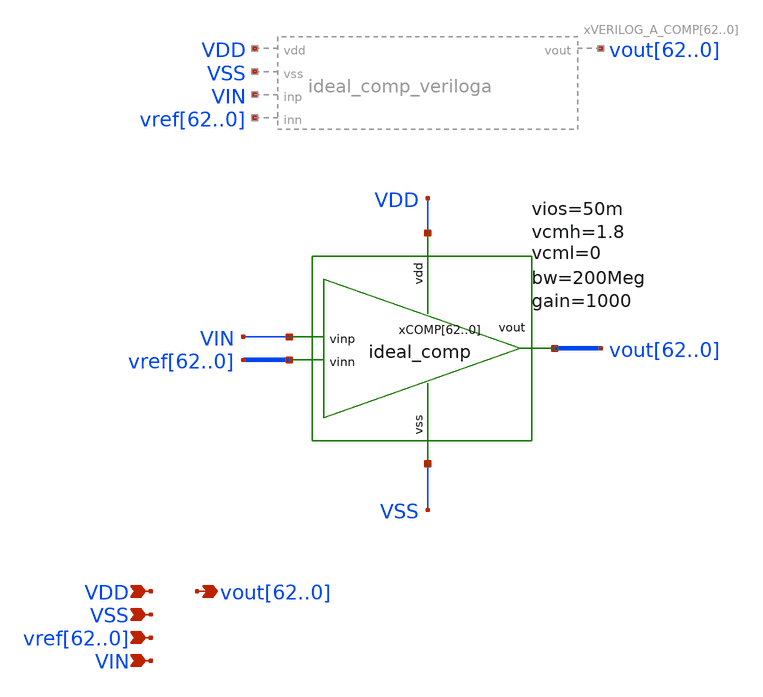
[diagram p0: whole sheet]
** sch_path: schematics/comp_top_ideal.sch
**.subckt comp_top_ideal
*+ vout62,vout61,vout60,vout59,vout58,vout57,vout56,vout55,vout54,vout53,vout52,vout51,vout50,vout49,vout48,vout47,vout46,vout45,vout44,vout43,vout42,vout41,vout40,vout39,vout38,vout37,vout36,vout35,vout34,vout33,vout32,vout31,vout30,vout29,vout28,vout27,vout26,vout25,vout24,vout23,vout22,vout21,vout20,vout19,vout18,vout17,vout16,vout15,vout14,vout13,vout12,vout11,vout10,vout9,vout8,vout7,vout6,vout5,vout4,vout3,vout2,vout1,vout0 VDD VSS
*+ vref62,vref61,vref60,vref59,vref58,vref57,vref56,vref55,vref54,vref53,vref52,vref51,vref50,vref49,vref48,vref47,vref46,vref45,vref44,vref43,vref42,vref41,vref40,vref39,vref38,vref37,vref36,vref35,vref34,vref33,vref32,vref31,vref30,vref29,vref28,vref27,vref26,vref25,vref24,vref23,vref22,vref21,vref20,vref19,vref18,vref17,vref16,vref15,vref14,vref13,vref12,vref11,vref10,vref9,vref8,vref7,vref6,vref5,vref4,vref3,vref2,vref1,vref0 VIN
*.opin
*+ vout62,vout61,vout60,vout59,vout58,vout57,vout56,vout55,vout54,vout53,vout52,vout51,vout50,vout49,vout48,vout47,vout46,vout45,vout44,vout43,vout42,vout41,vout40,vout39,vout38,vout37,vout36,vout35,vout34,vout33,vout32,vout31,vout30,vout29,vout28,vout27,vout26,vout25,vout24,vout23,vout22,vout21,vout20,vout19,vout18,vout17,vout16,vout15,vout14,vout13,vout12,vout11,vout10,vout9,vout8,vout7,vout6,vout5,vout4,vout3,vout2,vout1,vout0
*.ipin VDD
*.ipin VSS
*.ipin
*+ vref62,vref61,vref60,vref59,vref58,vref57,vref56,vref55,vref54,vref53,vref52,vref51,vref50,vref49,vref48,vref47,vref46,vref45,vref44,vref43,vref42,vref41,vref40,vref39,vref38,vref37,vref36,vref35,vref34,vref33,vref32,vref31,vref30,vref29,vref28,vref27,vref26,vref25,vref24,vref23,vref22,vref21,vref20,vref19,vref18,vref17,vref16,vref15,vref14,vref13,vref12,vref11,vref10,vref9,vref8,vref7,vref6,vref5,vref4,vref3,vref2,vref1,vref0
*.ipin VIN
xCOMP62 VDD VSS VIN vout62 vref62 ideal_comp bw=200Meg gain=1000 vdd= vss= vcmh=1.8 vcml=0 vios=50m
xCOMP61 VDD VSS VIN vout61 vref61 ideal_comp bw=200Meg gain=1000 vdd= vss= vcmh=1.8 vcml=0 vios=50m
xCOMP60 VDD VSS VIN vout60 vref60 ideal_comp bw=200Meg gain=1000 vdd= vss= vcmh=1.8 vcml=0 vios=50m
xCOMP59 VDD VSS VIN vout59 vref59 ideal_comp bw=200Meg gain=1000 vdd= vss= vcmh=1.8 vcml=0 vios=50m
xCOMP58 VDD VSS VIN vout58 vref58 ideal_comp bw=200Meg gain=1000 vdd= vss= vcmh=1.8 vcml=0 vios=50m
xCOMP57 VDD VSS VIN vout57 vref57 ideal_comp bw=200Meg gain=1000 vdd= vss= vcmh=1.8 vcml=0 vios=50m
xCOMP56 VDD VSS VIN vout56 vref56 ideal_comp bw=200Meg gain=1000 vdd= vss= vcmh=1.8 vcml=0 vios=50m
xCOMP55 VDD VSS VIN vout55 vref55 ideal_comp bw=200Meg gain=1000 vdd= vss= vcmh=1.8 vcml=0 vios=50m
xCOMP54 VDD VSS VIN vout54 vref54 ideal_comp bw=200Meg gain=1000 vdd= vss= vcmh=1.8 vcml=0 vios=50m
xCOMP53 VDD VSS VIN vout53 vref53 ideal_comp bw=200Meg gain=1000 vdd= vss= vcmh=1.8 vcml=0 vios=50m
xCOMP52 VDD VSS VIN vout52 vref52 ideal_comp bw=200Meg gain=1000 vdd= vss= vcmh=1.8 vcml=0 vios=50m
xCOMP51 VDD VSS VIN vout51 vref51 ideal_comp bw=200Meg gain=1000 vdd= vss= vcmh=1.8 vcml=0 vios=50m
xCOMP50 VDD VSS VIN vout50 vref50 ideal_comp bw=200Meg gain=1000 vdd= vss= vcmh=1.8 vcml=0 vios=50m
xCOMP49 VDD VSS VIN vout49 vref49 ideal_comp bw=200Meg gain=1000 vdd= vss= vcmh=1.8 vcml=0 vios=50m
xCOMP48 VDD VSS VIN vout48 vref48 ideal_comp bw=200Meg gain=1000 vdd= vss= vcmh=1.8 vcml=0 vios=50m
xCOMP47 VDD VSS VIN vout47 vref47 ideal_comp bw=200Meg gain=1000 vdd= vss= vcmh=1.8 vcml=0 vios=50m
xCOMP46 VDD VSS VIN vout46 vref46 ideal_comp bw=200Meg gain=1000 vdd= vss= vcmh=1.8 vcml=0 vios=50m
xCOMP45 VDD VSS VIN vout45 vref45 ideal_comp bw=200Meg gain=1000 vdd= vss= vcmh=1.8 vcml=0 vios=50m
xCOMP44 VDD VSS VIN vout44 vref44 ideal_comp bw=200Meg gain=1000 vdd= vss= vcmh=1.8 vcml=0 vios=50m
xCOMP43 VDD VSS VIN vout43 vref43 ideal_comp bw=200Meg gain=1000 vdd= vss= vcmh=1.8 vcml=0 vios=50m
xCOMP42 VDD VSS VIN vout42 vref42 ideal_comp bw=200Meg gain=1000 vdd= vss= vcmh=1.8 vcml=0 vios=50m
xCOMP41 VDD VSS VIN vout41 vref41 ideal_comp bw=200Meg gain=1000 vdd= vss= vcmh=1.8 vcml=0 vios=50m
xCOMP40 VDD VSS VIN vout40 vref40 ideal_comp bw=200Meg gain=1000 vdd= vss= vcmh=1.8 vcml=0 vios=50m
xCOMP39 VDD VSS VIN vout39 vref39 ideal_comp bw=200Meg gain=1000 vdd= vss= vcmh=1.8 vcml=0 vios=50m
xCOMP38 VDD VSS VIN vout38 vref38 ideal_comp bw=200Meg gain=1000 vdd= vss= vcmh=1.8 vcml=0 vios=50m
xCOMP37 VDD VSS VIN vout37 vref37 ideal_comp bw=200Meg gain=1000 vdd= vss= vcmh=1.8 vcml=0 vios=50m
xCOMP36 VDD VSS VIN vout36 vref36 ideal_comp bw=200Meg gain=1000 vdd= vss= vcmh=1.8 vcml=0 vios=50m
xCOMP35 VDD VSS VIN vout35 vref35 ideal_comp bw=200Meg gain=1000 vdd= vss= vcmh=1.8 vcml=0 vios=50m
xCOMP34 VDD VSS VIN vout34 vref34 ideal_comp bw=200Meg gain=1000 vdd= vss= vcmh=1.8 vcml=0 vios=50m
xCOMP33 VDD VSS VIN vout33 vref33 ideal_comp bw=200Meg gain=1000 vdd= vss= vcmh=1.8 vcml=0 vios=50m
xCOMP32 VDD VSS VIN vout32 vref32 ideal_comp bw=200Meg gain=1000 vdd= vss= vcmh=1.8 vcml=0 vios=50m
xCOMP31 VDD VSS VIN vout31 vref31 ideal_comp bw=200Meg gain=1000 vdd= vss= vcmh=1.8 vcml=0 vios=50m
xCOMP30 VDD VSS VIN vout30 vref30 ideal_comp bw=200Meg gain=1000 vdd= vss= vcmh=1.8 vcml=0 vios=50m
xCOMP29 VDD VSS VIN vout29 vref29 ideal_comp bw=200Meg gain=1000 vdd= vss= vcmh=1.8 vcml=0 vios=50m
xCOMP28 VDD VSS VIN vout28 vref28 ideal_comp bw=200Meg gain=1000 vdd= vss= vcmh=1.8 vcml=0 vios=50m
xCOMP27 VDD VSS VIN vout27 vref27 ideal_comp bw=200Meg gain=1000 vdd= vss= vcmh=1.8 vcml=0 vios=50m
xCOMP26 VDD VSS VIN vout26 vref26 ideal_comp bw=200Meg gain=1000 vdd= vss= vcmh=1.8 vcml=0 vios=50m
xCOMP25 VDD VSS VIN vout25 vref25 ideal_comp bw=200Meg gain=1000 vdd= vss= vcmh=1.8 vcml=0 vios=50m
xCOMP24 VDD VSS VIN vout24 vref24 ideal_comp bw=200Meg gain=1000 vdd= vss= vcmh=1.8 vcml=0 vios=50m
xCOMP23 VDD VSS VIN vout23 vref23 ideal_comp bw=200Meg gain=1000 vdd= vss= vcmh=1.8 vcml=0 vios=50m
xCOMP22 VDD VSS VIN vout22 vref22 ideal_comp bw=200Meg gain=1000 vdd= vss= vcmh=1.8 vcml=0 vios=50m
xCOMP21 VDD VSS VIN vout21 vref21 ideal_comp bw=200Meg gain=1000 vdd= vss= vcmh=1.8 vcml=0 vios=50m
xCOMP20 VDD VSS VIN vout20 vref20 ideal_comp bw=200Meg gain=1000 vdd= vss= vcmh=1.8 vcml=0 vios=50m
xCOMP19 VDD VSS VIN vout19 vref19 ideal_comp bw=200Meg gain=1000 vdd= vss= vcmh=1.8 vcml=0 vios=50m
xCOMP18 VDD VSS VIN vout18 vref18 ideal_comp bw=200Meg gain=1000 vdd= vss= vcmh=1.8 vcml=0 vios=50m
xCOMP17 VDD VSS VIN vout17 vref17 ideal_comp bw=200Meg gain=1000 vdd= vss= vcmh=1.8 vcml=0 vios=50m
xCOMP16 VDD VSS VIN vout16 vref16 ideal_comp bw=200Meg gain=1000 vdd= vss= vcmh=1.8 vcml=0 vios=50m
xCOMP15 VDD VSS VIN vout15 vref15 ideal_comp bw=200Meg gain=1000 vdd= vss= vcmh=1.8 vcml=0 vios=50m
xCOMP14 VDD VSS VIN vout14 vref14 ideal_comp bw=200Meg gain=1000 vdd= vss= vcmh=1.8 vcml=0 vios=50m
xCOMP13 VDD VSS VIN vout13 vref13 ideal_comp bw=200Meg gain=1000 vdd= vss= vcmh=1.8 vcml=0 vios=50m
xCOMP12 VDD VSS VIN vout12 vref12 ideal_comp bw=200Meg gain=1000 vdd= vss= vcmh=1.8 vcml=0 vios=50m
xCOMP11 VDD VSS VIN vout11 vref11 ideal_comp bw=200Meg gain=1000 vdd= vss= vcmh=1.8 vcml=0 vios=50m
xCOMP10 VDD VSS VIN vout10 vref10 ideal_comp bw=200Meg gain=1000 vdd= vss= vcmh=1.8 vcml=0 vios=50m
xCOMP9 VDD VSS VIN vout9 vref9 ideal_comp bw=200Meg gain=1000 vdd= vss= vcmh=1.8 vcml=0 vios=50m
xCOMP8 VDD VSS VIN vout8 vref8 ideal_comp bw=200Meg gain=1000 vdd= vss= vcmh=1.8 vcml=0 vios=50m
xCOMP7 VDD VSS VIN vout7 vref7 ideal_comp bw=200Meg gain=1000 vdd= vss= vcmh=1.8 vcml=0 vios=50m
xCOMP6 VDD VSS VIN vout6 vref6 ideal_comp bw=200Meg gain=1000 vdd= vss= vcmh=1.8 vcml=0 vios=50m
xCOMP5 VDD VSS VIN vout5 vref5 ideal_comp bw=200Meg gain=1000 vdd= vss= vcmh=1.8 vcml=0 vios=50m
xCOMP4 VDD VSS VIN vout4 vref4 ideal_comp bw=200Meg gain=1000 vdd= vss= vcmh=1.8 vcml=0 vios=50m
xCOMP3 VDD VSS VIN vout3 vref3 ideal_comp bw=200Meg gain=1000 vdd= vss= vcmh=1.8 vcml=0 vios=50m
xCOMP2 VDD VSS VIN vout2 vref2 ideal_comp bw=200Meg gain=1000 vdd= vss= vcmh=1.8 vcml=0 vios=50m
xCOMP1 VDD VSS VIN vout1 vref1 ideal_comp bw=200Meg gain=1000 vdd= vss= vcmh=1.8 vcml=0 vios=50m
xCOMP0 VDD VSS VIN vout0 vref0 ideal_comp bw=200Meg gain=1000 vdd= vss= vcmh=1.8 vcml=0 vios=50m
**.ends

* expanding   symbol:  schematics/ideal_comp.sym # of pins=5
** sym_path: schematics/ideal_comp.sym
** sch_path: schematics/ideal_comp.sch
.subckt ideal_comp vdd vss vinp vout vinn  bw=200Meg gain=1000 vcmh=1.8 vcml=0 vios=50m
*.ipin vdd
*.opin vout
*.ipin vss
*.ipin vinp
*.ipin vinn
B1 vp vss V = {V(vinp)<vcmh ? (V(vinp) < vcml ? vcml: V(vinp)) : vcmh}
B2 vn vss V = {V(vinn)<vcmh ? (V(vinn) < vcml ? vcml: V(vinn) + vios) : vcmh}
B3 net1 vss V = {gain*(V(vp)-V(vn)) < V(vdd) ? (gain*(V(vp)-V(vn)) < V(vss) ? V(vss) : (gain*(V(vp)-V(vn)))) : V(vdd)}
R1 vout net1 {1/(2*3.1415*bw*1p)} m=1
C1 vout vss 1p m=1
.ends

.end
